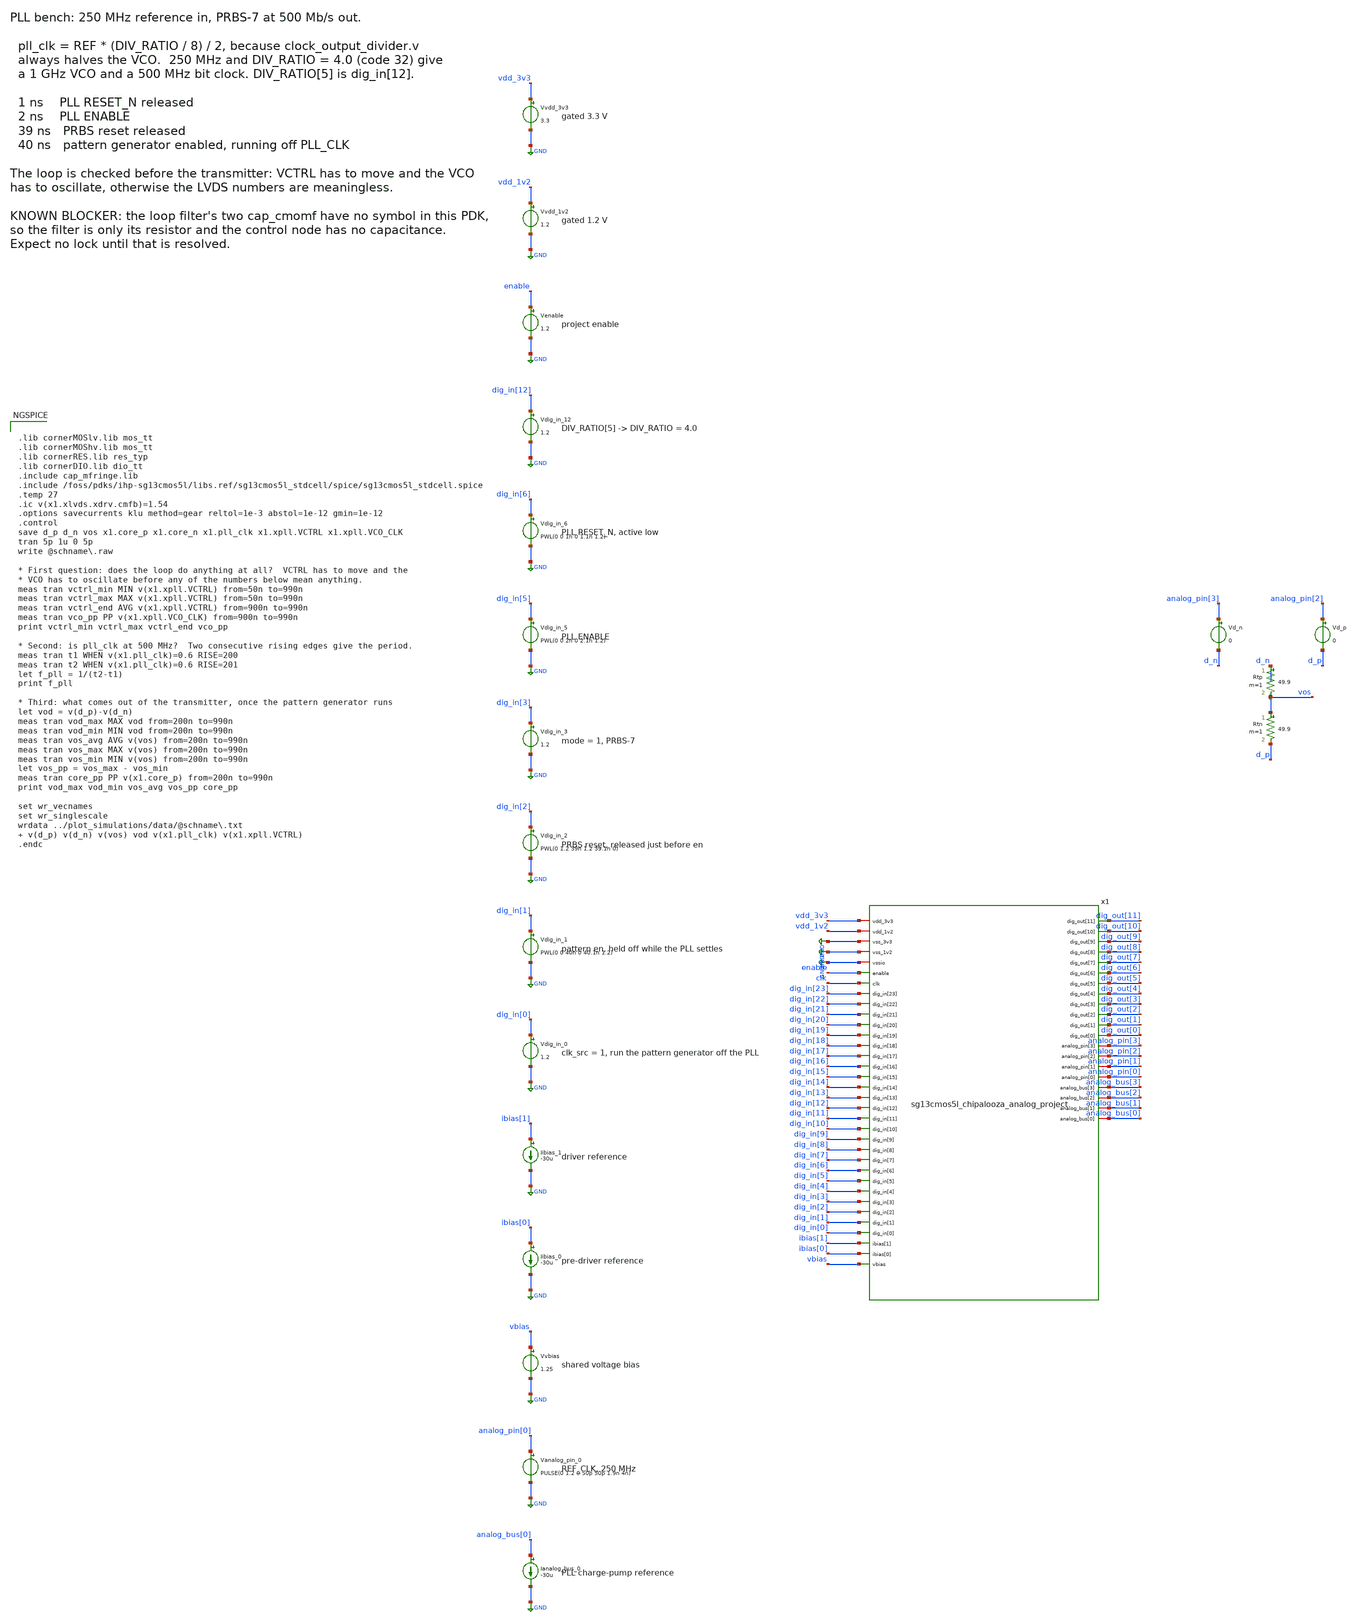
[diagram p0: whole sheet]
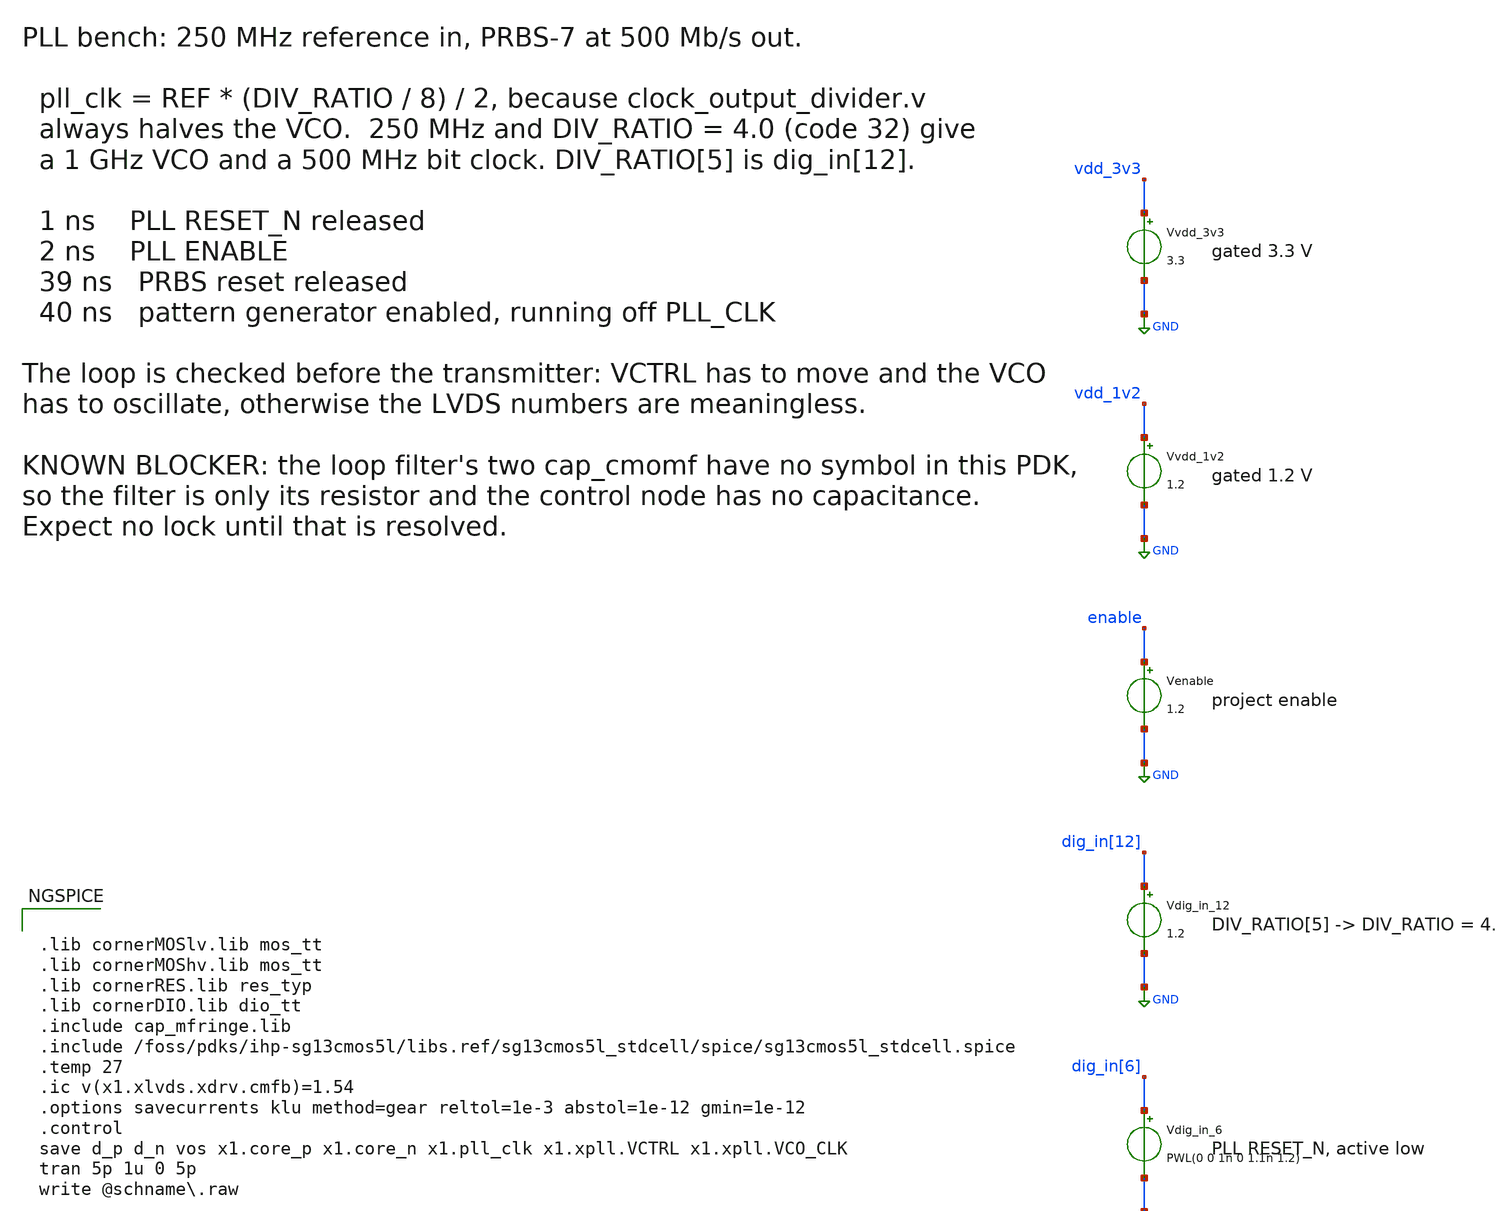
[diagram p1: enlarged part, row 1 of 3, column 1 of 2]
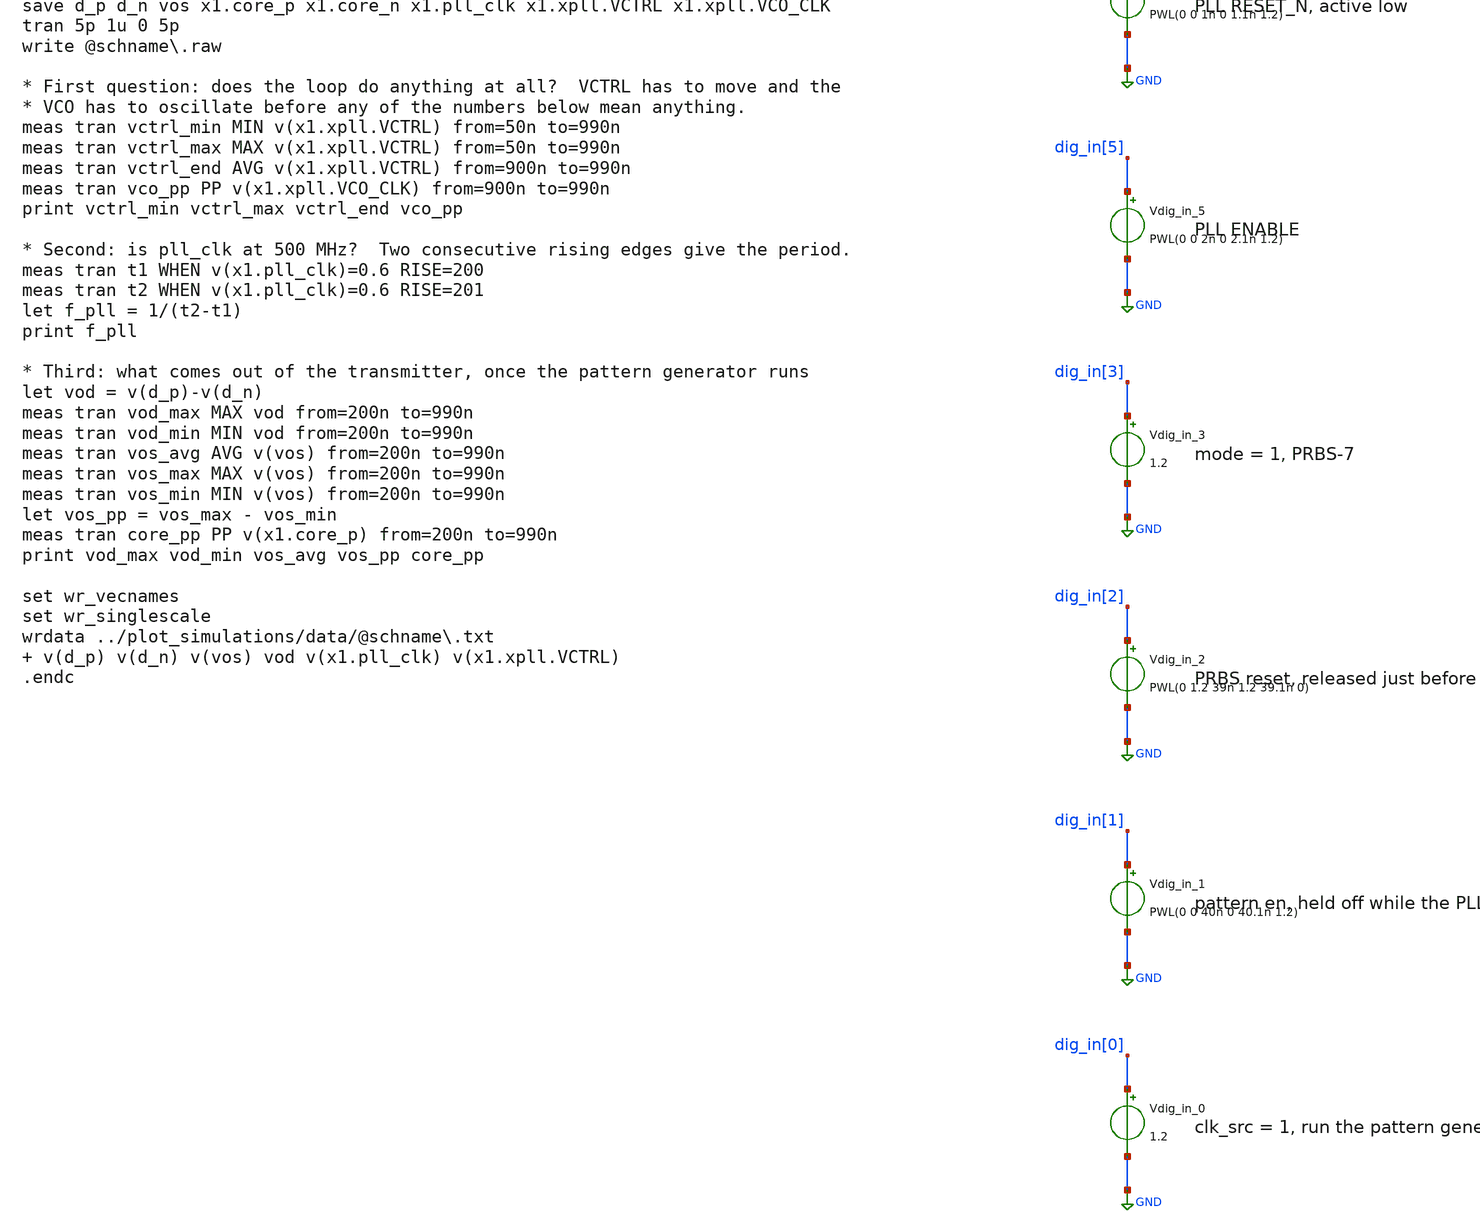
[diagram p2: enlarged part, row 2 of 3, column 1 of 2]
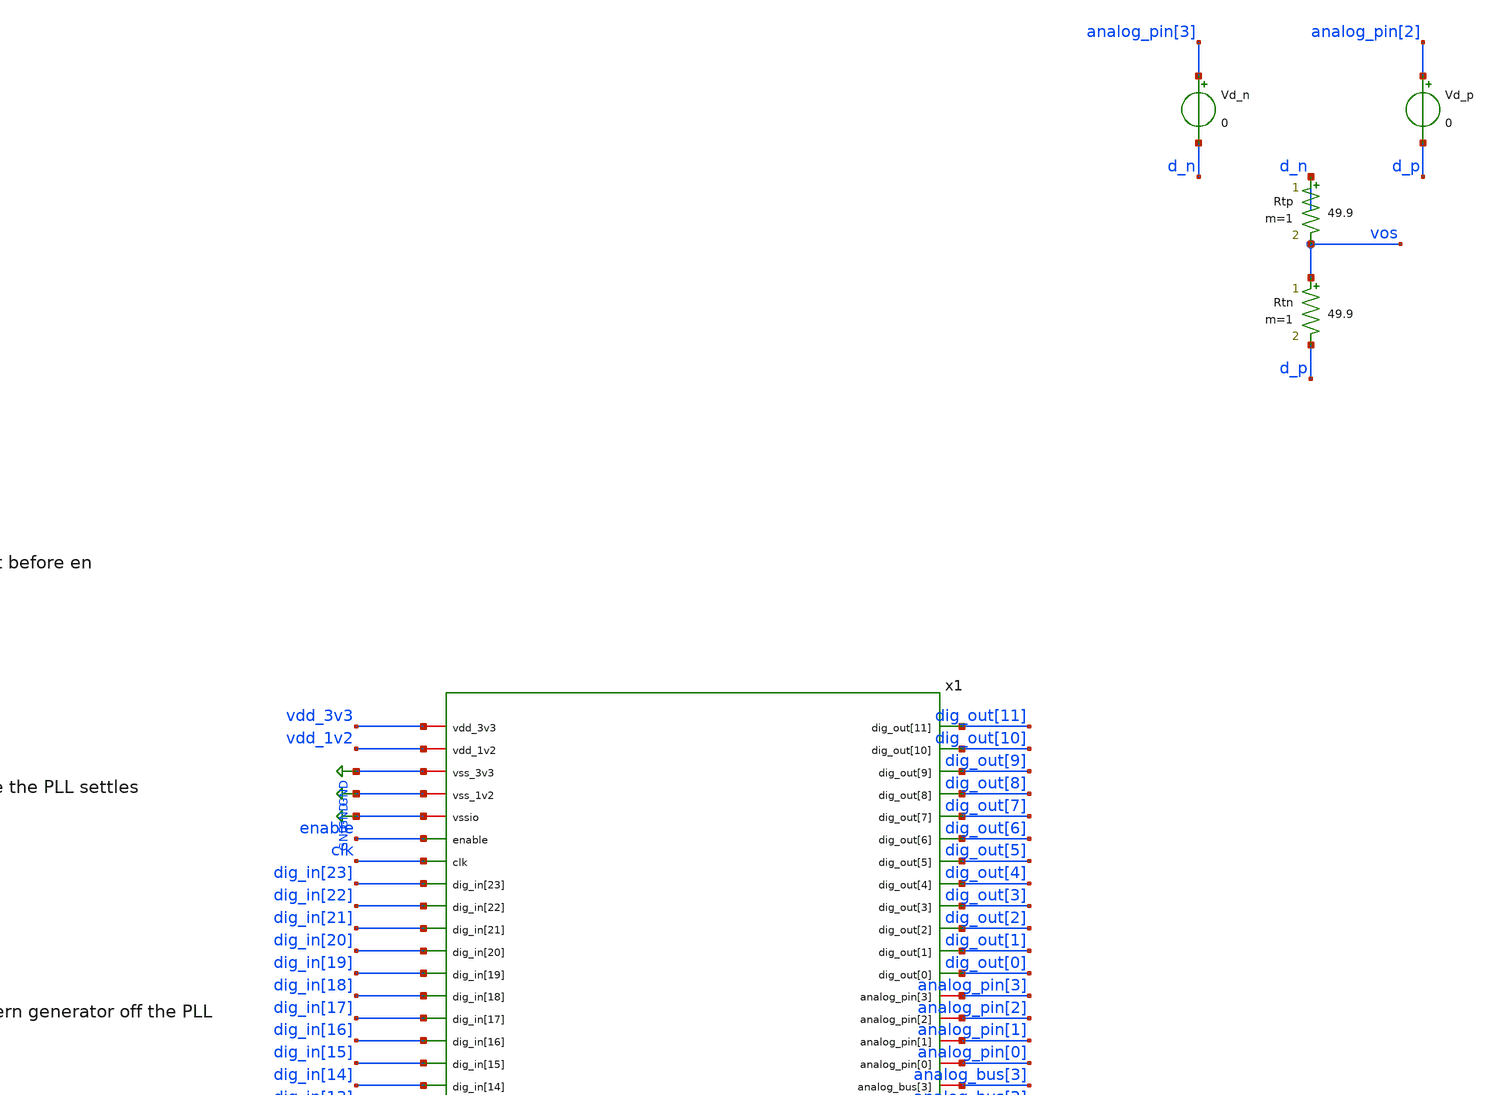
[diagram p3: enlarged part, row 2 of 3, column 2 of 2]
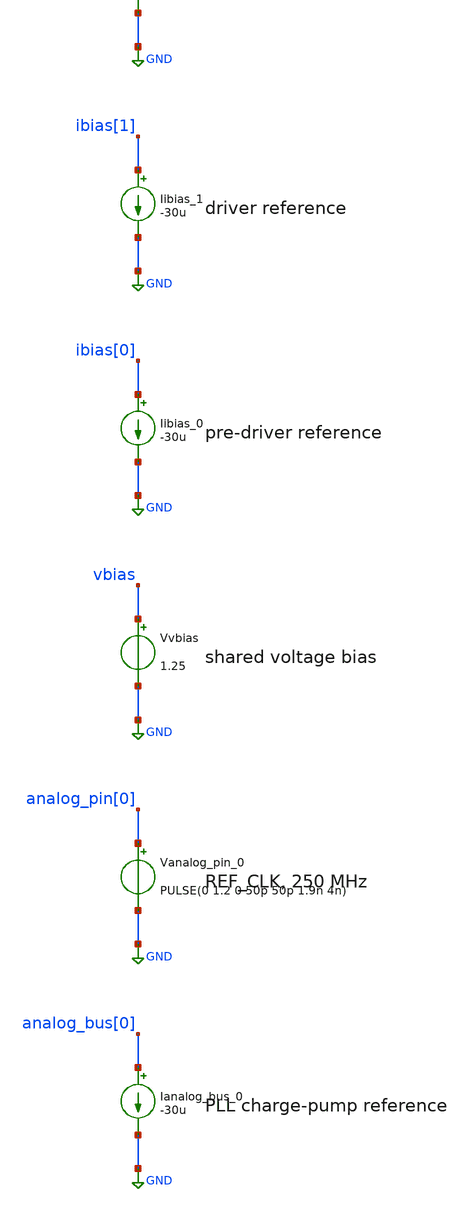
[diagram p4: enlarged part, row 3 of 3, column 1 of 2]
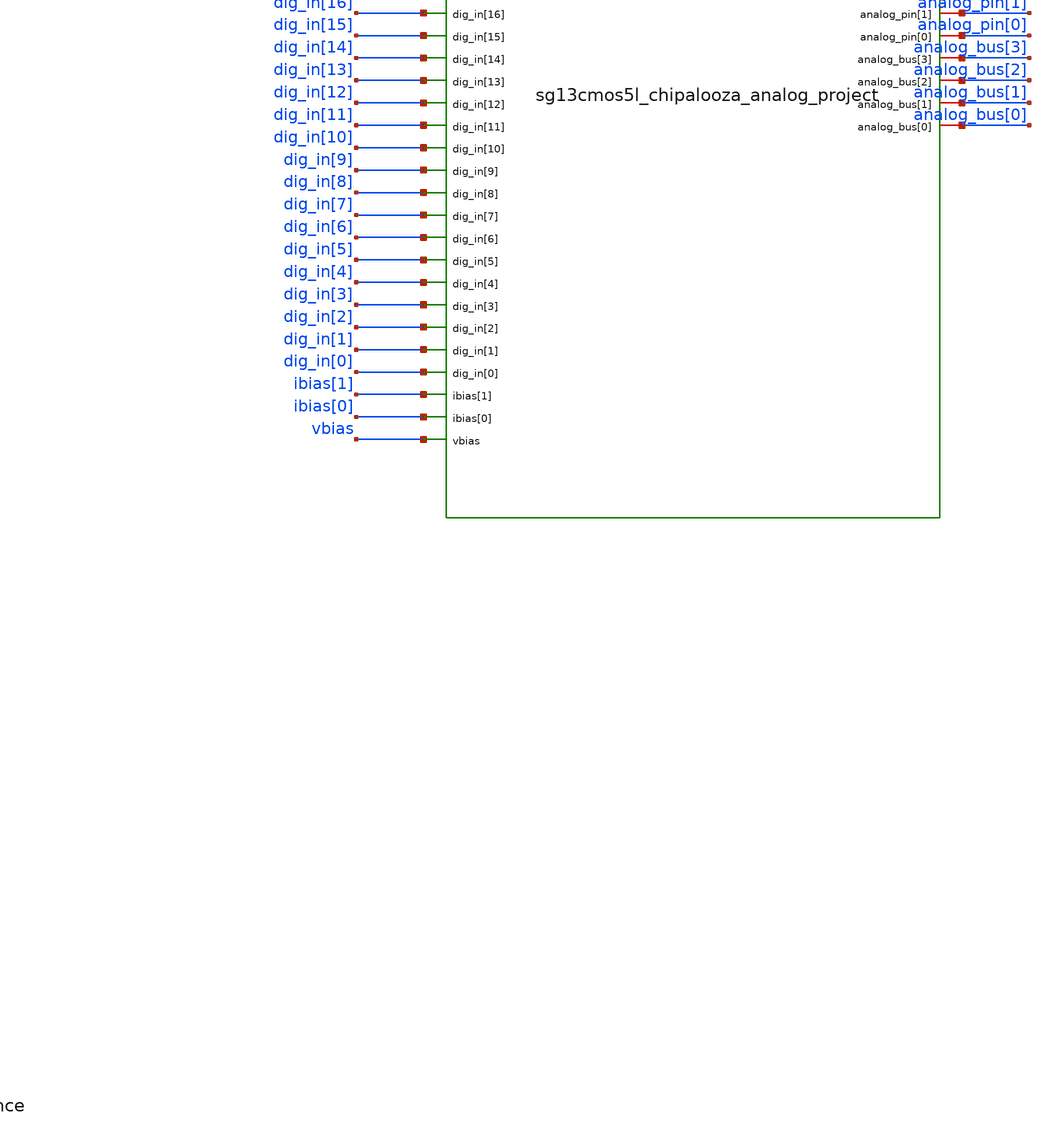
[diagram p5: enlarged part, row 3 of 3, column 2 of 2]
** sch_path: testbenches/xschem/sg13cmos5l_chipalooza_analog_project_tb_pll.sch
**.subckt sg13cmos5l_chipalooza_analog_project_tb_pll
Vvdd_3v3 vdd_3v3 GND 3.3
Vvdd_1v2 vdd_1v2 GND 1.2
Venable enable GND 1.2
Vdig_in_12 dig_in[12] GND 1.2
Vdig_in_6 dig_in[6] GND PWL(0 0 1n 0 1.1n 1.2)
Vdig_in_5 dig_in[5] GND PWL(0 0 2n 0 2.1n 1.2)
Vdig_in_3 dig_in[3] GND 1.2
Vdig_in_2 dig_in[2] GND PWL(0 1.2 39n 1.2 39.1n 0)
Vdig_in_1 dig_in[1] GND PWL(0 0 40n 0 40.1n 1.2)
Vdig_in_0 dig_in[0] GND 1.2
Iibias_1 ibias[1] GND -30u
Iibias_0 ibias[0] GND -30u
Vvbias vbias GND 1.25
Vanalog_pin_0 analog_pin[0] GND PULSE(0 1.2 0 50p 50p 1.9n 4n)
Ianalog_bus_0 analog_bus[0] GND -30u
x1 vdd_3v3 vdd_1v2 GND GND GND enable clk dig_in[23] dig_in[22] dig_in[21] dig_in[20] dig_in[19]
+ dig_in[18] dig_in[17] dig_in[16] dig_in[15] dig_in[14] dig_in[13] dig_in[12] dig_in[11] dig_in[10] dig_in[9]
+ dig_in[8] dig_in[7] dig_in[6] dig_in[5] dig_in[4] dig_in[3] dig_in[2] dig_in[1] dig_in[0] ibias[1] ibias[0]
+ vbias dig_out[11] dig_out[10] dig_out[9] dig_out[8] dig_out[7] dig_out[6] dig_out[5] dig_out[4]
+ dig_out[3] dig_out[2] dig_out[1] dig_out[0] analog_pin[3] analog_pin[2] analog_pin[1] analog_pin[0]
+ analog_bus[3] analog_bus[2] analog_bus[1] analog_bus[0] sg13cmos5l_chipalooza_analog_project
Vd_n analog_pin[3] d_n 0
Vd_p analog_pin[2] d_p 0
Rtp d_n vos 49.9 m=1
Rtn vos d_p 49.9 m=1
**** begin user architecture code


.lib cornerMOSlv.lib mos_tt
.lib cornerMOShv.lib mos_tt
.lib cornerRES.lib res_typ
.lib cornerDIO.lib dio_tt
.include cap_mfringe.lib
.include /foss/pdks/ihp-sg13cmos5l/libs.ref/sg13cmos5l_stdcell/spice/sg13cmos5l_stdcell.spice
.temp 27
.ic v(x1.xlvds.xdrv.cmfb)=1.54
.options savecurrents klu method=gear reltol=1e-3 abstol=1e-12 gmin=1e-12
.control
save d_p d_n vos x1.core_p x1.core_n x1.pll_clk x1.xpll.VCTRL x1.xpll.VCO_CLK
tran 5p 1u 0 5p
write @schname\.raw

* First question: does the loop do anything at all?  VCTRL has to move and the
* VCO has to oscillate before any of the numbers below mean anything.
meas tran vctrl_min MIN v(x1.xpll.VCTRL) from=50n to=990n
meas tran vctrl_max MAX v(x1.xpll.VCTRL) from=50n to=990n
meas tran vctrl_end AVG v(x1.xpll.VCTRL) from=900n to=990n
meas tran vco_pp PP v(x1.xpll.VCO_CLK) from=900n to=990n
print vctrl_min vctrl_max vctrl_end vco_pp

* Second: is pll_clk at 500 MHz?  Two consecutive rising edges give the period.
meas tran t1 WHEN v(x1.pll_clk)=0.6 RISE=200
meas tran t2 WHEN v(x1.pll_clk)=0.6 RISE=201
let f_pll = 1/(t2-t1)
print f_pll

* Third: what comes out of the transmitter, once the pattern generator runs
let vod = v(d_p)-v(d_n)
meas tran vod_max MAX vod from=200n to=990n
meas tran vod_min MIN vod from=200n to=990n
meas tran vos_avg AVG v(vos) from=200n to=990n
meas tran vos_max MAX v(vos) from=200n to=990n
meas tran vos_min MIN v(vos) from=200n to=990n
let vos_pp = vos_max - vos_min
meas tran core_pp PP v(x1.core_p) from=200n to=990n
print vod_max vod_min vos_avg vos_pp core_pp

set wr_vecnames
set wr_singlescale
wrdata ../plot_simulations/data/@schname\.txt  v(d_p) v(d_n) v(vos) vod v(x1.pll_clk)
+ v(x1.xpll.VCTRL)
.endc


**** end user architecture code
**.ends
.GLOBAL GND
.end
